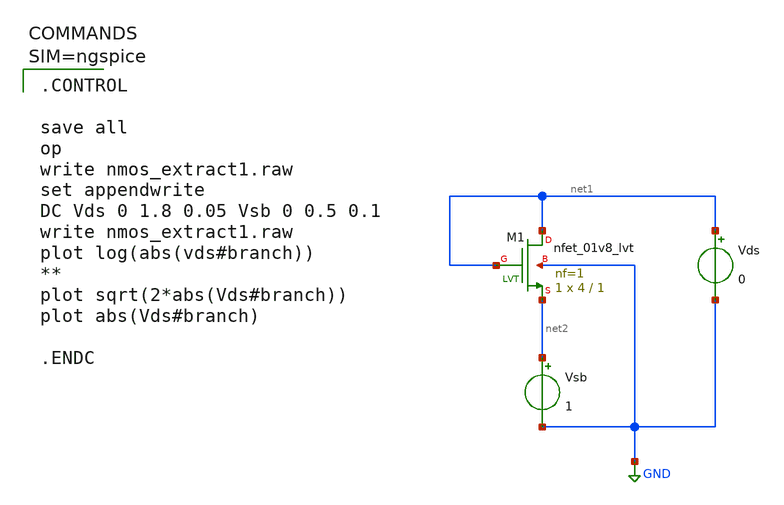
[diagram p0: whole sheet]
** sch_path: work/xschem/nmos_extract1.sch
**.subckt nmos_extract1
XM1 net1 net1 net2 GND sky130_fd_pr__nfet_01v8_lvt L=1 W=4 nf=1 ad='int((1 + 1)/2) * 4 / 1 * 0.29' as='int((1 + 2)/2) * 4 / 1 * 0.29'
+ pd='2*int((1 + 1)/2) * (4 / 1 + 0.29)' ps='2*int((1 + 2)/2) * (4 / 1 + 0.29)' nrd='0.29 / 4 ' nrs='0.29 / 4 '
+ sa=0 sb=0 sd=0 mult=1 m=1
Vsb net2 GND 1
Vds net1 GND 0
**** begin user architecture code


.CONTROL

save all
op
write nmos_extract1.raw
set appendwrite
DC Vds 0 1.8 0.05 Vsb 0 0.5 0.1
write nmos_extract1.raw
plot log(abs(vds#branch))
**
plot sqrt(2*abs(Vds#branch))
plot abs(Vds#branch)

.ENDC




** opencircuitdesign pdks install
.lib $::SKYWATER_MODELS/sky130.lib.spice tt

**** end user architecture code
**.ends
.GLOBAL GND
.end
